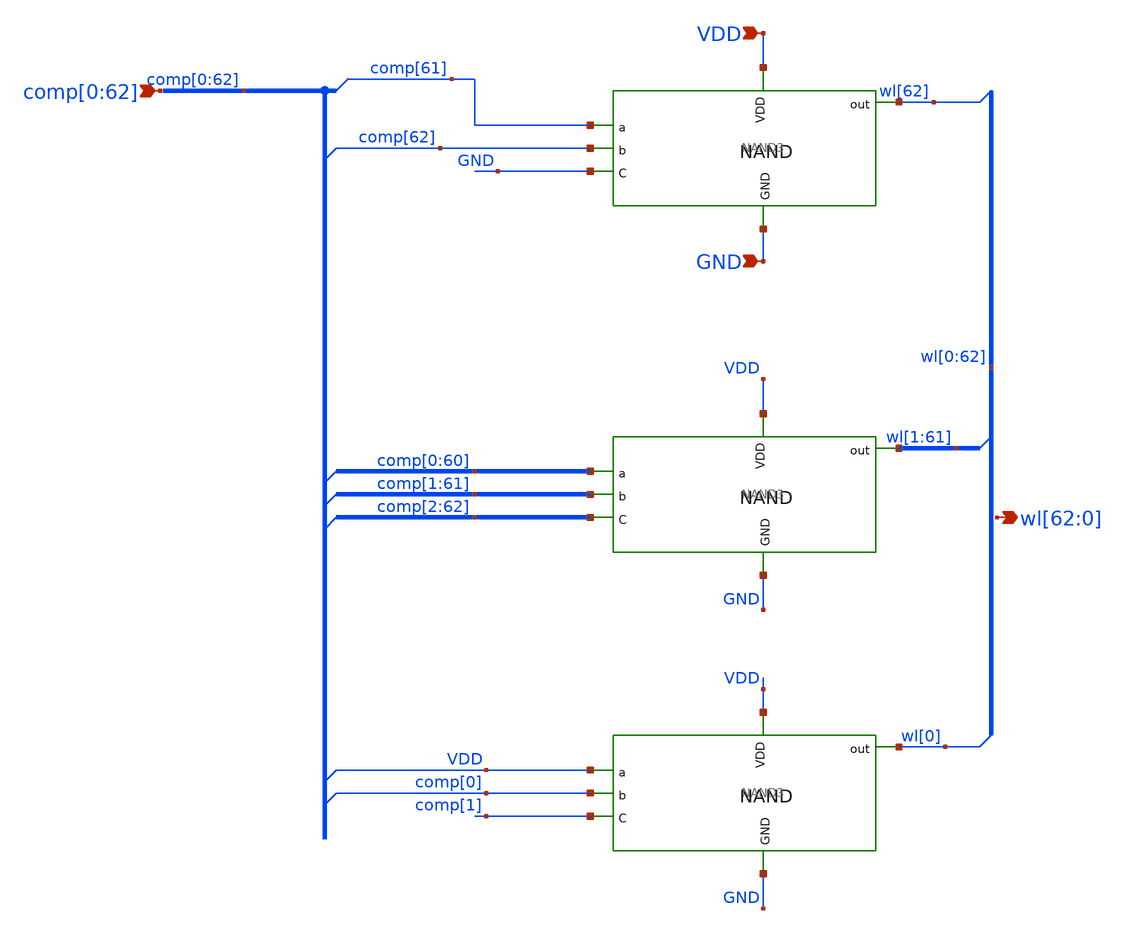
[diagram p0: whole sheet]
** sch_path: blocks/adc/encoder/sym/tm_to_bin2.sch
**.subckt tm_to_bin2
*+ wl[62],wl[61],wl[60],wl[59],wl[58],wl[57],wl[56],wl[55],wl[54],wl[53],wl[52],wl[51],wl[50],wl[49],wl[48],wl[47],wl[46],wl[45],wl[44],wl[43],wl[42],wl[41],wl[40],wl[39],wl[38],wl[37],wl[36],wl[35],wl[34],wl[33],wl[32],wl[31],wl[30],wl[29],wl[28],wl[27],wl[26],wl[25],wl[24],wl[23],wl[22],wl[21],wl[20],wl[19],wl[18],wl[17],wl[16],wl[15],wl[14],wl[13],wl[12],wl[11],wl[10],wl[9],wl[8],wl[7],wl[6],wl[5],wl[4],wl[3],wl[2],wl[1],wl[0]
*+ comp[0],comp[1],comp[2],comp[3],comp[4],comp[5],comp[6],comp[7],comp[8],comp[9],comp[10],comp[11],comp[12],comp[13],comp[14],comp[15],comp[16],comp[17],comp[18],comp[19],comp[20],comp[21],comp[22],comp[23],comp[24],comp[25],comp[26],comp[27],comp[28],comp[29],comp[30],comp[31],comp[32],comp[33],comp[34],comp[35],comp[36],comp[37],comp[38],comp[39],comp[40],comp[41],comp[42],comp[43],comp[44],comp[45],comp[46],comp[47],comp[48],comp[49],comp[50],comp[51],comp[52],comp[53],comp[54],comp[55],comp[56],comp[57],comp[58],comp[59],comp[60],comp[61],comp[62] VDD GND
*.opin
*+ wl[62],wl[61],wl[60],wl[59],wl[58],wl[57],wl[56],wl[55],wl[54],wl[53],wl[52],wl[51],wl[50],wl[49],wl[48],wl[47],wl[46],wl[45],wl[44],wl[43],wl[42],wl[41],wl[40],wl[39],wl[38],wl[37],wl[36],wl[35],wl[34],wl[33],wl[32],wl[31],wl[30],wl[29],wl[28],wl[27],wl[26],wl[25],wl[24],wl[23],wl[22],wl[21],wl[20],wl[19],wl[18],wl[17],wl[16],wl[15],wl[14],wl[13],wl[12],wl[11],wl[10],wl[9],wl[8],wl[7],wl[6],wl[5],wl[4],wl[3],wl[2],wl[1],wl[0]
*.ipin
*+ comp[0],comp[1],comp[2],comp[3],comp[4],comp[5],comp[6],comp[7],comp[8],comp[9],comp[10],comp[11],comp[12],comp[13],comp[14],comp[15],comp[16],comp[17],comp[18],comp[19],comp[20],comp[21],comp[22],comp[23],comp[24],comp[25],comp[26],comp[27],comp[28],comp[29],comp[30],comp[31],comp[32],comp[33],comp[34],comp[35],comp[36],comp[37],comp[38],comp[39],comp[40],comp[41],comp[42],comp[43],comp[44],comp[45],comp[46],comp[47],comp[48],comp[49],comp[50],comp[51],comp[52],comp[53],comp[54],comp[55],comp[56],comp[57],comp[58],comp[59],comp[60],comp[61],comp[62]
*.ipin VDD
*.ipin GND
x_top1 comp[62] comp[61] VDD wl[62] GND GND NAND3
x1[61] comp[1] comp[0] VDD wl[1] comp[2] GND NAND3
x1[60] comp[2] comp[1] VDD wl[2] comp[3] GND NAND3
x1[59] comp[3] comp[2] VDD wl[3] comp[4] GND NAND3
x1[58] comp[4] comp[3] VDD wl[4] comp[5] GND NAND3
x1[57] comp[5] comp[4] VDD wl[5] comp[6] GND NAND3
x1[56] comp[6] comp[5] VDD wl[6] comp[7] GND NAND3
x1[55] comp[7] comp[6] VDD wl[7] comp[8] GND NAND3
x1[54] comp[8] comp[7] VDD wl[8] comp[9] GND NAND3
x1[53] comp[9] comp[8] VDD wl[9] comp[10] GND NAND3
x1[52] comp[10] comp[9] VDD wl[10] comp[11] GND NAND3
x1[51] comp[11] comp[10] VDD wl[11] comp[12] GND NAND3
x1[50] comp[12] comp[11] VDD wl[12] comp[13] GND NAND3
x1[49] comp[13] comp[12] VDD wl[13] comp[14] GND NAND3
x1[48] comp[14] comp[13] VDD wl[14] comp[15] GND NAND3
x1[47] comp[15] comp[14] VDD wl[15] comp[16] GND NAND3
x1[46] comp[16] comp[15] VDD wl[16] comp[17] GND NAND3
x1[45] comp[17] comp[16] VDD wl[17] comp[18] GND NAND3
x1[44] comp[18] comp[17] VDD wl[18] comp[19] GND NAND3
x1[43] comp[19] comp[18] VDD wl[19] comp[20] GND NAND3
x1[42] comp[20] comp[19] VDD wl[20] comp[21] GND NAND3
x1[41] comp[21] comp[20] VDD wl[21] comp[22] GND NAND3
x1[40] comp[22] comp[21] VDD wl[22] comp[23] GND NAND3
x1[39] comp[23] comp[22] VDD wl[23] comp[24] GND NAND3
x1[38] comp[24] comp[23] VDD wl[24] comp[25] GND NAND3
x1[37] comp[25] comp[24] VDD wl[25] comp[26] GND NAND3
x1[36] comp[26] comp[25] VDD wl[26] comp[27] GND NAND3
x1[35] comp[27] comp[26] VDD wl[27] comp[28] GND NAND3
x1[34] comp[28] comp[27] VDD wl[28] comp[29] GND NAND3
x1[33] comp[29] comp[28] VDD wl[29] comp[30] GND NAND3
x1[32] comp[30] comp[29] VDD wl[30] comp[31] GND NAND3
x1[31] comp[31] comp[30] VDD wl[31] comp[32] GND NAND3
x1[30] comp[32] comp[31] VDD wl[32] comp[33] GND NAND3
x1[29] comp[33] comp[32] VDD wl[33] comp[34] GND NAND3
x1[28] comp[34] comp[33] VDD wl[34] comp[35] GND NAND3
x1[27] comp[35] comp[34] VDD wl[35] comp[36] GND NAND3
x1[26] comp[36] comp[35] VDD wl[36] comp[37] GND NAND3
x1[25] comp[37] comp[36] VDD wl[37] comp[38] GND NAND3
x1[24] comp[38] comp[37] VDD wl[38] comp[39] GND NAND3
x1[23] comp[39] comp[38] VDD wl[39] comp[40] GND NAND3
x1[22] comp[40] comp[39] VDD wl[40] comp[41] GND NAND3
x1[21] comp[41] comp[40] VDD wl[41] comp[42] GND NAND3
x1[20] comp[42] comp[41] VDD wl[42] comp[43] GND NAND3
x1[19] comp[43] comp[42] VDD wl[43] comp[44] GND NAND3
x1[18] comp[44] comp[43] VDD wl[44] comp[45] GND NAND3
x1[17] comp[45] comp[44] VDD wl[45] comp[46] GND NAND3
x1[16] comp[46] comp[45] VDD wl[46] comp[47] GND NAND3
x1[15] comp[47] comp[46] VDD wl[47] comp[48] GND NAND3
x1[14] comp[48] comp[47] VDD wl[48] comp[49] GND NAND3
x1[13] comp[49] comp[48] VDD wl[49] comp[50] GND NAND3
x1[12] comp[50] comp[49] VDD wl[50] comp[51] GND NAND3
x1[11] comp[51] comp[50] VDD wl[51] comp[52] GND NAND3
x1[10] comp[52] comp[51] VDD wl[52] comp[53] GND NAND3
x1[9] comp[53] comp[52] VDD wl[53] comp[54] GND NAND3
x1[8] comp[54] comp[53] VDD wl[54] comp[55] GND NAND3
x1[7] comp[55] comp[54] VDD wl[55] comp[56] GND NAND3
x1[6] comp[56] comp[55] VDD wl[56] comp[57] GND NAND3
x1[5] comp[57] comp[56] VDD wl[57] comp[58] GND NAND3
x1[4] comp[58] comp[57] VDD wl[58] comp[59] GND NAND3
x1[3] comp[59] comp[58] VDD wl[59] comp[60] GND NAND3
x1[2] comp[60] comp[59] VDD wl[60] comp[61] GND NAND3
x1[1] comp[61] comp[60] VDD wl[61] comp[62] GND NAND3
x_bot2 comp[0] VDD VDD wl[0] comp[1] GND NAND3
**.ends

* expanding   symbol:  blocks/adc/encoder/sym/NAND3.sym # of pins=6
** sym_path: blocks/adc/encoder/sym/NAND3.sym
** sch_path: blocks/adc/encoder/sym/NAND3.sch
.subckt NAND3 b a VDD out C GND
*.ipin a
*.opin out
*.ipin C
*.ipin b
*.ipin VDD
*.ipin GND
XM5 out net1 VDD VDD pfet_03v3 L=0.28u W=0.22u nf=1 ad='int((nf+1)/2) * W/nf * 0.18u' as='int((nf+2)/2) * W/nf * 0.18u'
+ pd='2*int((nf+1)/2) * (W/nf + 0.18u)' ps='2*int((nf+2)/2) * (W/nf + 0.18u)' nrd='0.18u / W' nrs='0.18u / W'
+ sa=0 sb=0 sd=0 m=15
XM6 out net1 GND GND nfet_03v3 L=0.28u W=0.22u nf=1 ad='int((nf+1)/2) * W/nf * 0.18u' as='int((nf+2)/2) * W/nf * 0.18u'
+ pd='2*int((nf+1)/2) * (W/nf + 0.18u)' ps='2*int((nf+2)/2) * (W/nf + 0.18u)' nrd='0.18u / W' nrs='0.18u / W'
+ sa=0 sb=0 sd=0 m=7
XM7 cbar C VDD VDD pfet_03v3 L=0.28u W=0.22u nf=1 ad='int((nf+1)/2) * W/nf * 0.18u' as='int((nf+2)/2) * W/nf * 0.18u'
+ pd='2*int((nf+1)/2) * (W/nf + 0.18u)' ps='2*int((nf+2)/2) * (W/nf + 0.18u)' nrd='0.18u / W' nrs='0.18u / W'
+ sa=0 sb=0 sd=0 m=15
XM8 cbar C GND GND nfet_03v3 L=0.28u W=0.22u nf=1 ad='int((nf+1)/2) * W/nf * 0.18u' as='int((nf+2)/2) * W/nf * 0.18u'
+ pd='2*int((nf+1)/2) * (W/nf + 0.18u)' ps='2*int((nf+2)/2) * (W/nf + 0.18u)' nrd='0.18u / W' nrs='0.18u / W'
+ sa=0 sb=0 sd=0 m=7
XM13 net1 a VDD VDD pfet_03v3 L=0.28u W=0.22u nf=1 ad='int((nf+1)/2) * W/nf * 0.18u' as='int((nf+2)/2) * W/nf * 0.18u'
+ pd='2*int((nf+1)/2) * (W/nf + 0.18u)' ps='2*int((nf+2)/2) * (W/nf + 0.18u)' nrd='0.18u / W' nrs='0.18u / W'
+ sa=0 sb=0 sd=0 m=15
XM14 net1 b VDD VDD pfet_03v3 L=0.28u W=0.22u nf=1 ad='int((nf+1)/2) * W/nf * 0.18u' as='int((nf+2)/2) * W/nf * 0.18u'
+ pd='2*int((nf+1)/2) * (W/nf + 0.18u)' ps='2*int((nf+2)/2) * (W/nf + 0.18u)' nrd='0.18u / W' nrs='0.18u / W'
+ sa=0 sb=0 sd=0 m=15
XM15 net1 cbar VDD VDD pfet_03v3 L=0.28u W=0.22u nf=1 ad='int((nf+1)/2) * W/nf * 0.18u' as='int((nf+2)/2) * W/nf * 0.18u'
+ pd='2*int((nf+1)/2) * (W/nf + 0.18u)' ps='2*int((nf+2)/2) * (W/nf + 0.18u)' nrd='0.18u / W' nrs='0.18u / W'
+ sa=0 sb=0 sd=0 m=15
XM16 net1 a net2 GND nfet_03v3 L=0.28u W=0.22u nf=1 ad='int((nf+1)/2) * W/nf * 0.18u' as='int((nf+2)/2) * W/nf * 0.18u'
+ pd='2*int((nf+1)/2) * (W/nf + 0.18u)' ps='2*int((nf+2)/2) * (W/nf + 0.18u)' nrd='0.18u / W' nrs='0.18u / W'
+ sa=0 sb=0 sd=0 m=7
XM17 net2 b net3 GND nfet_03v3 L=0.28u W=0.22u nf=1 ad='int((nf+1)/2) * W/nf * 0.18u' as='int((nf+2)/2) * W/nf * 0.18u'
+ pd='2*int((nf+1)/2) * (W/nf + 0.18u)' ps='2*int((nf+2)/2) * (W/nf + 0.18u)' nrd='0.18u / W' nrs='0.18u / W'
+ sa=0 sb=0 sd=0 m=7
XM18 net3 cbar GND GND nfet_03v3 L=0.28u W=0.22u nf=1 ad='int((nf+1)/2) * W/nf * 0.18u' as='int((nf+2)/2) * W/nf * 0.18u'
+ pd='2*int((nf+1)/2) * (W/nf + 0.18u)' ps='2*int((nf+2)/2) * (W/nf + 0.18u)' nrd='0.18u / W' nrs='0.18u / W'
+ sa=0 sb=0 sd=0 m=7
.ends

.end
